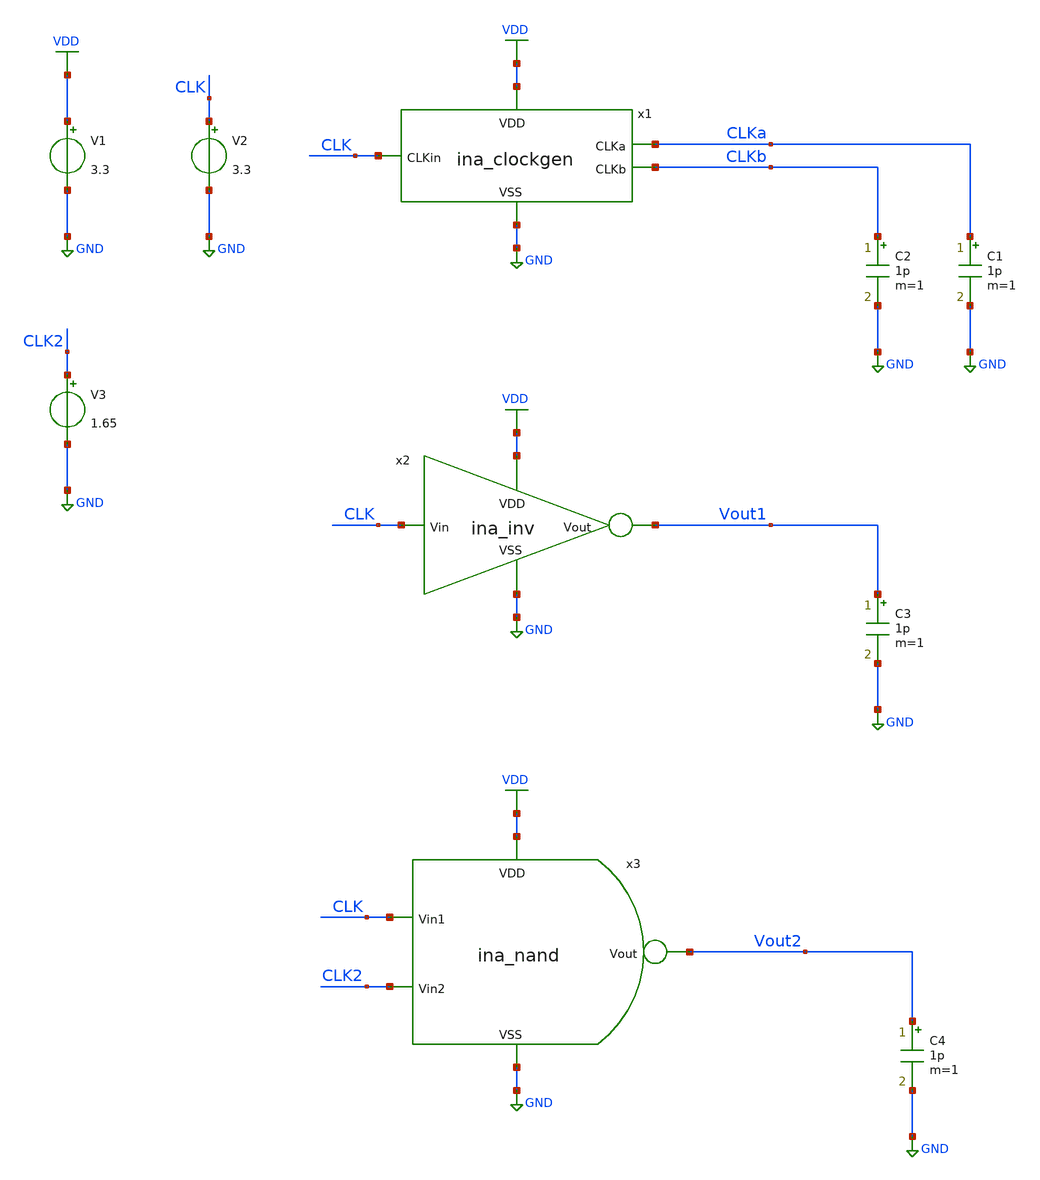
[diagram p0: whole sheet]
** sch_path: designs/libs/tb_ina/tb_ina_clockgen_tran/tb_ina_clockgen_tran.sch
**.subckt tb_ina_clockgen_tran
V1 VDD GND 3.3
C2 CLKb GND 1p m=1
C1 CLKa GND 1p m=1
V2 CLK GND 3.3
x1 VDD CLK CLKa CLKb GND ina_clockgen
x2 VDD CLK Vout1 GND ina_inv
C3 Vout1 GND 1p m=1
C4 Vout2 GND 1p m=1
x3 VDD Vout2 CLK CLK2 GND ina_nand
V3 CLK2 GND 1.65
**** begin user architecture code

.include $::180MCU_MODELS/design.ngspice
.lib $::180MCU_MODELS/sm141064.ngspice typical
.lib $::180MCU_MODELS/sm141064.ngspice cap_mim
.lib $::180MCU_MODELS/sm141064.ngspice moscap_typical
.lib $::180MCU_MODELS/sm141064.ngspice mimcap_typical
.lib $::180MCU_MODELS/sm141064.ngspice res_typical
* .lib $::180MCU_MODELS/sm141064.ngspice res_statistical
* ngspice commands




.control
save all

run
set color0 = white

*************************************
** INPUT CLOCK PARAMETERS
*************************************

let Vdd = 3.3
let fchop = 4k
let tper = 1/fchop
let ton = tper/2
let tr = 10n
let tf = 10n
let tper2 = 2*tper
let ton2 = tper2/2

*************************************
** TRANSIENT PARAMETERS
*************************************

let tstop = 600u
let tstep = 10n

*************************************
** SOURCES
*************************************

alter @V1[DC] = $&Vdd
alter @V2[PULSE] = [ 0 $&Vdd 0 $&tr $&tf $&ton $&tper 0 ]
alter @V3[PULSE] = [ $&Vdd 0 0 $&tr $&tf $&ton2 $&tper2 0 ]

*************************************
** TRANSIENT SIMULATION
*************************************

tran $&tstep $&tstop

*************************************
** PLOTS
*************************************

setplot tran1
let vclk = v(CLK)
let vclka = v(CLKa)
let vclkb = v(CLKb)
let vclk2 = v(CLK2)
let vout1 = v(Vout1)
let vout2 = v(Vout2)
plot vclk
plot vclka vclkb
plot vclka+vclkb
plot vclk vout1
plot vclk2 vout2

*************************************
** SAVE
*************************************

write tb_ina_clockgen_tran.raw

.endc
* ngspice commands



**** end user architecture code
**.ends

* expanding   symbol:  libs/core_ina/ina_clockgen/ina_clockgen.sym # of pins=5
** sym_path: designs/libs/core_ina/ina_clockgen/ina_clockgen.sym
** sch_path: designs/libs/core_ina/ina_clockgen/ina_clockgen.sch
.subckt ina_clockgen VDD CLKin CLKa CLKb VSS
*.ipin CLKin
*.ipin VDD
*.ipin VSS
*.opin CLKa
*.opin CLKb
x1 VDD net4 CLKin net1 VSS ina_nand
x2 VDD net6 net3 net2 VSS ina_nand
x3 VDD CLKin net2 VSS ina_inv
x4 VDD net4 net5 VSS ina_inv
x5 VDD net5 net3 VSS ina_inv
x6 VDD net3 CLKa VSS ina_inv
x7 VDD net6 net7 VSS ina_inv
x8 VDD net7 net1 VSS ina_inv
x9 VDD net1 CLKb VSS ina_inv
.ends


* expanding   symbol:  libs/core_ina/ina_inv/ina_inv.sym # of pins=4
** sym_path: designs/libs/core_ina/ina_inv/ina_inv.sym
** sch_path: designs/libs/core_ina/ina_inv/ina_inv.sch
.subckt ina_inv VDD Vin Vout VSS
*.ipin VDD
*.ipin VSS
*.ipin Vin
*.opin Vout
XMI1 Vout Vin VDD VDD pfet_03v3 L=0.28u W=2u nf=1 ad='int((nf+1)/2) * W/nf * 0.18u' as='int((nf+2)/2) * W/nf * 0.18u'
+ pd='2*int((nf+1)/2) * (W/nf + 0.18u)' ps='2*int((nf+2)/2) * (W/nf + 0.18u)' nrd='0.18u / W' nrs='0.18u / W'
+ sa=0 sb=0 sd=0 m=1
XMI2 Vout Vin VSS VSS nfet_03v3 L=0.28u W=1u nf=1 ad='int((nf+1)/2) * W/nf * 0.18u' as='int((nf+2)/2) * W/nf * 0.18u'
+ pd='2*int((nf+1)/2) * (W/nf + 0.18u)' ps='2*int((nf+2)/2) * (W/nf + 0.18u)' nrd='0.18u / W' nrs='0.18u / W'
+ sa=0 sb=0 sd=0 m=1
.ends


* expanding   symbol:  libs/core_ina/ina_nand/ina_nand.sym # of pins=5
** sym_path: designs/libs/core_ina/ina_nand/ina_nand.sym
** sch_path: designs/libs/core_ina/ina_nand/ina_nand.sch
.subckt ina_nand VDD Vout Vin1 Vin2 VSS
*.ipin VDD
*.ipin Vin1
*.ipin Vin2
*.ipin VSS
*.opin Vout
XMN1 Vout Vin1 VDD VDD pfet_03v3 L=0.28u W=2u nf=1 ad='int((nf+1)/2) * W/nf * 0.18u' as='int((nf+2)/2) * W/nf * 0.18u'
+ pd='2*int((nf+1)/2) * (W/nf + 0.18u)' ps='2*int((nf+2)/2) * (W/nf + 0.18u)' nrd='0.18u / W' nrs='0.18u / W'
+ sa=0 sb=0 sd=0 m=1
XMN2 Vout Vin2 VDD VDD pfet_03v3 L=0.28u W=2u nf=1 ad='int((nf+1)/2) * W/nf * 0.18u' as='int((nf+2)/2) * W/nf * 0.18u'
+ pd='2*int((nf+1)/2) * (W/nf + 0.18u)' ps='2*int((nf+2)/2) * (W/nf + 0.18u)' nrd='0.18u / W' nrs='0.18u / W'
+ sa=0 sb=0 sd=0 m=1
XMN3 Vout Vin1 net1 VSS nfet_03v3 L=0.28u W=2u nf=1 ad='int((nf+1)/2) * W/nf * 0.18u' as='int((nf+2)/2) * W/nf * 0.18u'
+ pd='2*int((nf+1)/2) * (W/nf + 0.18u)' ps='2*int((nf+2)/2) * (W/nf + 0.18u)' nrd='0.18u / W' nrs='0.18u / W'
+ sa=0 sb=0 sd=0 m=1
XMN4 net1 Vin2 VSS VSS nfet_03v3 L=0.28u W=2u nf=1 ad='int((nf+1)/2) * W/nf * 0.18u' as='int((nf+2)/2) * W/nf * 0.18u'
+ pd='2*int((nf+1)/2) * (W/nf + 0.18u)' ps='2*int((nf+2)/2) * (W/nf + 0.18u)' nrd='0.18u / W' nrs='0.18u / W'
+ sa=0 sb=0 sd=0 m=1
.ends

.GLOBAL GND
.GLOBAL VDD
.end
